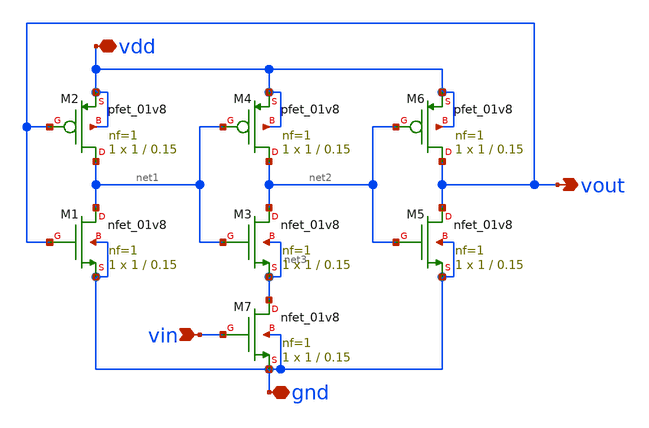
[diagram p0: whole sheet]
** sch_path: vc_oscillator/vc_oscillator.sch
**.subckt vc_oscillator vdd gnd vin vout
*.iopin vdd
*.iopin gnd
*.ipin vin
*.opin vout
XM1 net1 vout gnd gnd sky130_fd_pr__nfet_01v8 L=0.15 W=1 nf=1 ad='int((nf+1)/2) * W/nf * 0.29' as='int((nf+2)/2) * W/nf * 0.29'
+ pd='2*int((nf+1)/2) * (W/nf + 0.29)' ps='2*int((nf+2)/2) * (W/nf + 0.29)' nrd='0.29 / W' nrs='0.29 / W'
+ sa=0 sb=0 sd=0 mult=1 m=1
XM2 net1 vout vdd vdd sky130_fd_pr__pfet_01v8 L=0.15 W=1 nf=1 ad='int((nf+1)/2) * W/nf * 0.29' as='int((nf+2)/2) * W/nf * 0.29'
+ pd='2*int((nf+1)/2) * (W/nf + 0.29)' ps='2*int((nf+2)/2) * (W/nf + 0.29)' nrd='0.29 / W' nrs='0.29 / W'
+ sa=0 sb=0 sd=0 mult=1 m=1
XM3 net2 net1 net3 net3 sky130_fd_pr__nfet_01v8 L=0.15 W=1 nf=1 ad='int((nf+1)/2) * W/nf * 0.29' as='int((nf+2)/2) * W/nf * 0.29'
+ pd='2*int((nf+1)/2) * (W/nf + 0.29)' ps='2*int((nf+2)/2) * (W/nf + 0.29)' nrd='0.29 / W' nrs='0.29 / W'
+ sa=0 sb=0 sd=0 mult=1 m=1
XM4 net2 net1 vdd vdd sky130_fd_pr__pfet_01v8 L=0.15 W=1 nf=1 ad='int((nf+1)/2) * W/nf * 0.29' as='int((nf+2)/2) * W/nf * 0.29'
+ pd='2*int((nf+1)/2) * (W/nf + 0.29)' ps='2*int((nf+2)/2) * (W/nf + 0.29)' nrd='0.29 / W' nrs='0.29 / W'
+ sa=0 sb=0 sd=0 mult=1 m=1
XM5 vout net2 gnd gnd sky130_fd_pr__nfet_01v8 L=0.15 W=1 nf=1 ad='int((nf+1)/2) * W/nf * 0.29' as='int((nf+2)/2) * W/nf * 0.29'
+ pd='2*int((nf+1)/2) * (W/nf + 0.29)' ps='2*int((nf+2)/2) * (W/nf + 0.29)' nrd='0.29 / W' nrs='0.29 / W'
+ sa=0 sb=0 sd=0 mult=1 m=1
XM6 vout net2 vdd vdd sky130_fd_pr__pfet_01v8 L=0.15 W=1 nf=1 ad='int((nf+1)/2) * W/nf * 0.29' as='int((nf+2)/2) * W/nf * 0.29'
+ pd='2*int((nf+1)/2) * (W/nf + 0.29)' ps='2*int((nf+2)/2) * (W/nf + 0.29)' nrd='0.29 / W' nrs='0.29 / W'
+ sa=0 sb=0 sd=0 mult=1 m=1
XM7 net3 vin gnd gnd sky130_fd_pr__nfet_01v8 L=0.15 W=1 nf=1 ad='int((nf+1)/2) * W/nf * 0.29' as='int((nf+2)/2) * W/nf * 0.29'
+ pd='2*int((nf+1)/2) * (W/nf + 0.29)' ps='2*int((nf+2)/2) * (W/nf + 0.29)' nrd='0.29 / W' nrs='0.29 / W'
+ sa=0 sb=0 sd=0 mult=1 m=1
**.ends
.end
